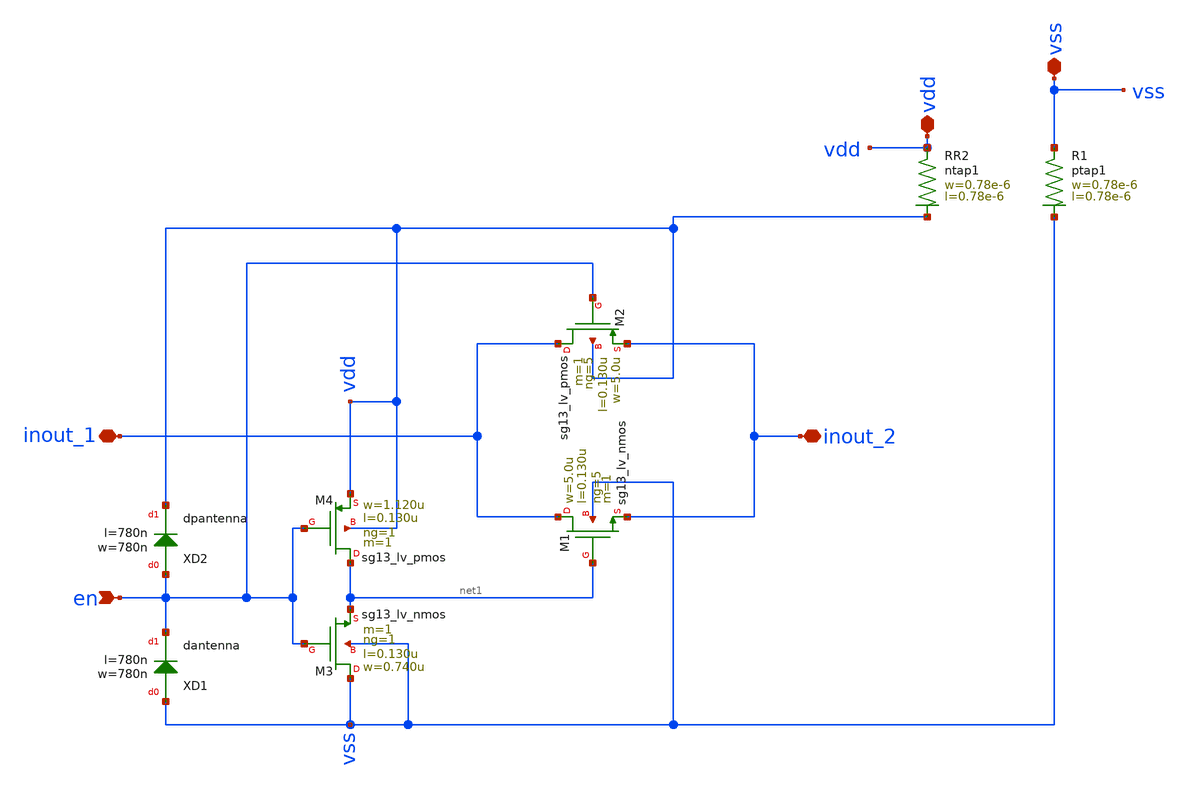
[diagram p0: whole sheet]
** sch_path: AnalogLDO_exampleDesign/design_data/klayout/netlist/tgate.sch
**.subckt tgate inout_1 inout_2 en vdd vss
*.iopin inout_1
*.iopin inout_2
*.ipin en
*.iopin vdd
*.iopin vss
XM1 inout_1 net1 inout_2 vss sg13_lv_nmos w=5.0u l=0.130u ng=5 m=1 mm_ok=1
XM2 inout_1 en inout_2 vdd sg13_lv_pmos w=5.0u l=0.130u ng=5 m=1 mm_ok=1
XR1 vss vss ptap1 R=262.8 w=0.78e-6 l=0.78e-6
XR2 vdd vdd ntap1 R=262.8 w=0.78e-6 l=0.78e-6
XM3 vss en net1 vss sg13_lv_nmos w=0.740u l=0.130u ng=1 m=1 mm_ok=1
XM4 net1 en vdd vdd sg13_lv_pmos w=1.120u l=0.130u ng=1 m=1 mm_ok=1
XXD1 vss en dantenna l=780n w=780n
XXD2 en vdd dpantenna l=780n w=780n
**.ends
.end
